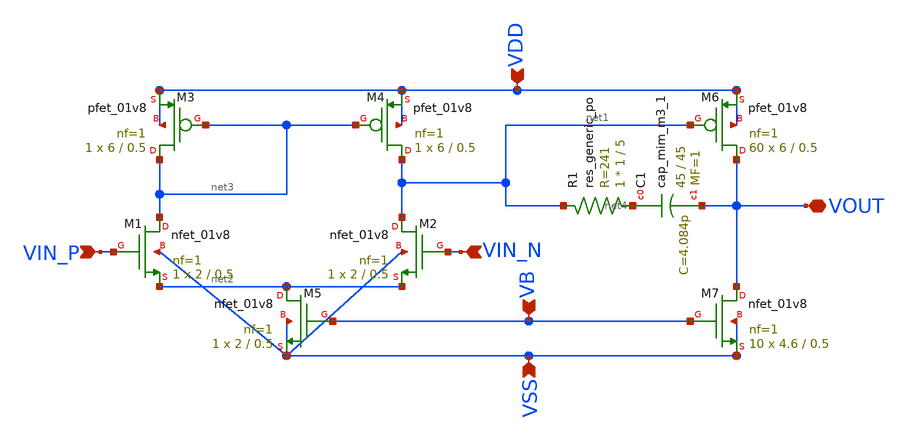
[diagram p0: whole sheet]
** sch_path: analog/bootcamp_opamp/build/schematic/onboarding.sch
**.subckt onboarding VIN_P VDD VSS VB VIN_N VOUT
*.ipin VIN_P
*.ipin VDD
*.ipin VSS
*.ipin VB
*.ipin VIN_N
*.iopin VOUT
XC1 net4 VOUT sky130_fd_pr__cap_mim_m3_1 W=45 L=45 MF=1 m=1
XM6 VOUT net1 VDD VDD sky130_fd_pr__pfet_01v8 L=0.5 W=6 nf=1 ad='int((nf+1)/2) * W/nf * 0.29' as='int((nf+2)/2) * W/nf * 0.29'
+ pd='2*int((nf+1)/2) * (W/nf + 0.29)' ps='2*int((nf+2)/2) * (W/nf + 0.29)' nrd='0.29 / W' nrs='0.29 / W'
+ sa=0 sb=0 sd=0 mult=60 m=60
XM1 net3 VIN_P net2 VSS sky130_fd_pr__nfet_01v8 L=0.5 W=2 nf=1 ad='int((nf+1)/2) * W/nf * 0.29' as='int((nf+2)/2) * W/nf * 0.29'
+ pd='2*int((nf+1)/2) * (W/nf + 0.29)' ps='2*int((nf+2)/2) * (W/nf + 0.29)' nrd='0.29 / W' nrs='0.29 / W'
+ sa=0 sb=0 sd=0 mult=1 m=1
XM2 net1 VIN_N net2 VSS sky130_fd_pr__nfet_01v8 L=0.5 W=2 nf=1 ad='int((nf+1)/2) * W/nf * 0.29' as='int((nf+2)/2) * W/nf * 0.29'
+ pd='2*int((nf+1)/2) * (W/nf + 0.29)' ps='2*int((nf+2)/2) * (W/nf + 0.29)' nrd='0.29 / W' nrs='0.29 / W'
+ sa=0 sb=0 sd=0 mult=1 m=1
XM4 net1 net3 VDD VDD sky130_fd_pr__pfet_01v8 L=0.5 W=6 nf=1 ad='int((nf+1)/2) * W/nf * 0.29' as='int((nf+2)/2) * W/nf * 0.29'
+ pd='2*int((nf+1)/2) * (W/nf + 0.29)' ps='2*int((nf+2)/2) * (W/nf + 0.29)' nrd='0.29 / W' nrs='0.29 / W'
+ sa=0 sb=0 sd=0 mult=1 m=1
XM3 net3 net3 VDD VDD sky130_fd_pr__pfet_01v8 L=0.5 W=6 nf=1 ad='int((nf+1)/2) * W/nf * 0.29' as='int((nf+2)/2) * W/nf * 0.29'
+ pd='2*int((nf+1)/2) * (W/nf + 0.29)' ps='2*int((nf+2)/2) * (W/nf + 0.29)' nrd='0.29 / W' nrs='0.29 / W'
+ sa=0 sb=0 sd=0 mult=1 m=1
XM5 net2 VB VSS VSS sky130_fd_pr__nfet_01v8 L=0.5 W=2 nf=1 ad='int((nf+1)/2) * W/nf * 0.29' as='int((nf+2)/2) * W/nf * 0.29'
+ pd='2*int((nf+1)/2) * (W/nf + 0.29)' ps='2*int((nf+2)/2) * (W/nf + 0.29)' nrd='0.29 / W' nrs='0.29 / W'
+ sa=0 sb=0 sd=0 mult=1 m=1
XM7 VOUT VB VSS VSS sky130_fd_pr__nfet_01v8 L=0.5 W=4.6 nf=1 ad='int((nf+1)/2) * W/nf * 0.29' as='int((nf+2)/2) * W/nf * 0.29'
+ pd='2*int((nf+1)/2) * (W/nf + 0.29)' ps='2*int((nf+2)/2) * (W/nf + 0.29)' nrd='0.29 / W' nrs='0.29 / W'
+ sa=0 sb=0 sd=0 mult=10 m=10
XR1 net4 net1 sky130_fd_pr__res_generic_po W=1 L=5 m=1
**.ends
.end
